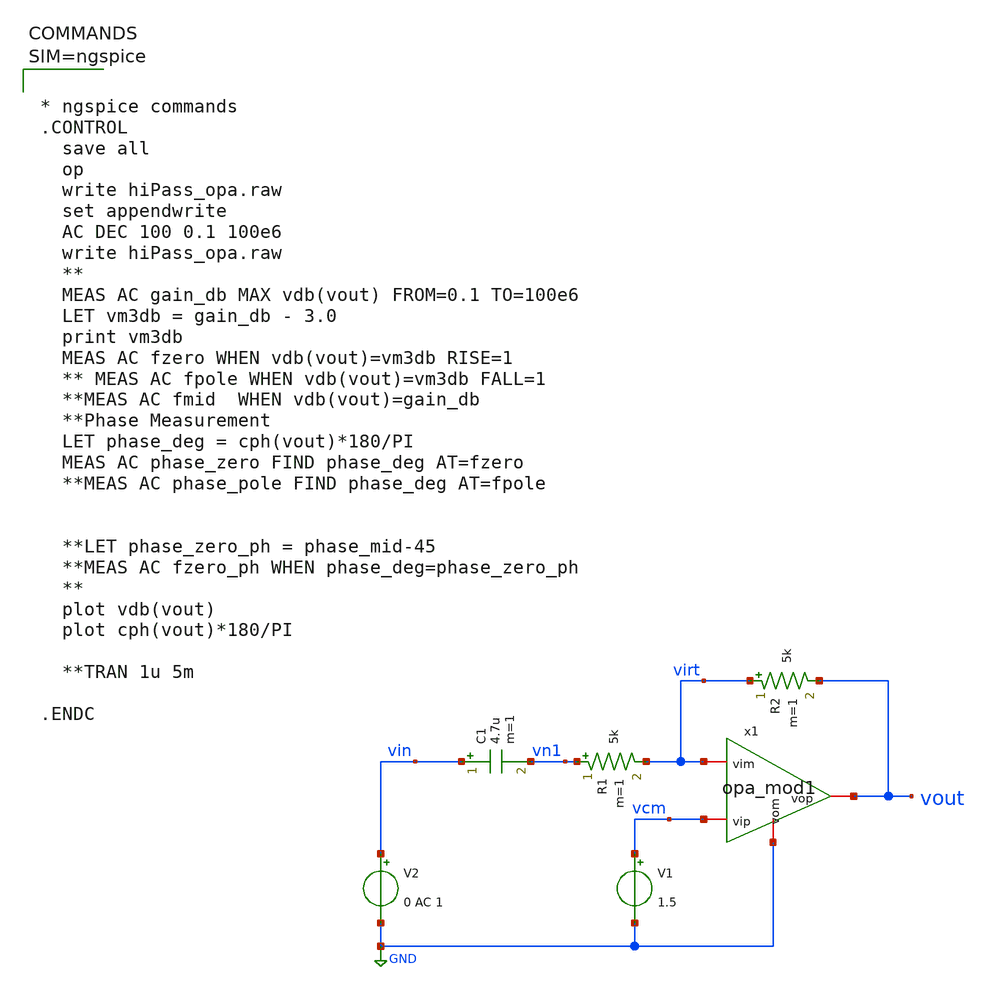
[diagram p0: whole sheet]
** sch_path: xschem/hiPass_opa.sch
**.subckt hiPass_opa
x1 vout vcm virt GND opa_mod1
R1 vn1 virt 5k m=1
R2 virt vout 5k m=1
C1 vin vn1 4.7u m=1
V1 vcm GND 1.5
V2 vin GND 0 AC 1
**** begin user architecture code



* ngspice commands
.CONTROL
  save all
  op
  write hiPass_opa.raw
  set appendwrite
  AC DEC 100 0.1 100e6
  write hiPass_opa.raw
  **
  MEAS AC gain_db MAX vdb(vout) FROM=0.1 TO=100e6
  LET vm3db = gain_db - 3.0
  print vm3db
  MEAS AC fzero WHEN vdb(vout)=vm3db RISE=1
  ** MEAS AC fpole WHEN vdb(vout)=vm3db FALL=1
  **MEAS AC fmid  WHEN vdb(vout)=gain_db
  **Phase Measurement
  LET phase_deg = cph(vout)*180/PI
  MEAS AC phase_zero FIND phase_deg AT=fzero
  **MEAS AC phase_pole FIND phase_deg AT=fpole


  **LET phase_zero_ph = phase_mid-45
  **MEAS AC fzero_ph WHEN phase_deg=phase_zero_ph
  **
  plot vdb(vout)
  plot cph(vout)*180/PI

  **TRAN 1u 5m

.ENDC



**** end user architecture code
**.ends

* expanding   symbol:  opa_mod1.sym # of pins=4
** sym_path: xschem/opa_mod1.sym
** sch_path: xschem/opa_mod1.sch
.subckt opa_mod1 vop vip vim vom
*.iopin vop
*.iopin vom
*.iopin vip
*.iopin vim
E1 vilp GND vip vim 1000
R1 vilp volp 200 m=1
C1 volp GND 1u m=1
E2 vop vom volp GND 1
.ends

.GLOBAL GND
.end
